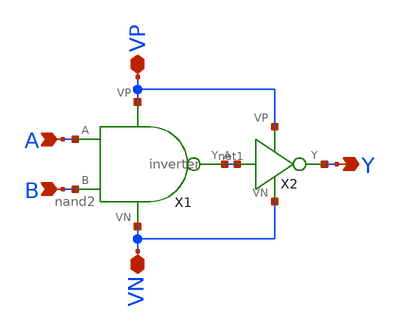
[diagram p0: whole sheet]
** sch_path: and2.sch
**.subckt and2 A B VP VN Y
*.ipin A
*.ipin B
*.iopin VP
*.iopin VN
*.opin Y
X1 B A net1 VP VN nand2
X2 net1 Y VP VN inverter
**.ends

* expanding   symbol:  /home/madvlsi/Documents/mp1/nand2.sym # of pins=5
** sym_path: nand2.sym
** sch_path: nand2.sch
.subckt nand2 B A Y VP VN
*.ipin A
*.ipin B
*.iopin VP
*.iopin VN
*.opin Y
XM1 Y A net1 VN sky130_fd_pr__nfet_01v8 L=0.15 W=1 nf=1 ad='int((nf+1)/2) * W/nf * 0.29' as='int((nf+2)/2) * W/nf * 0.29'
+ pd='2*int((nf+1)/2) * (W/nf + 0.29)' ps='2*int((nf+2)/2) * (W/nf + 0.29)' nrd='0.29 / W' nrs='0.29 / W'
+ sa=0 sb=0 sd=0 mult=1 m=1
XM2 net1 B VN VN sky130_fd_pr__nfet_01v8 L=0.15 W=1 nf=1 ad='int((nf+1)/2) * W/nf * 0.29' as='int((nf+2)/2) * W/nf * 0.29'
+ pd='2*int((nf+1)/2) * (W/nf + 0.29)' ps='2*int((nf+2)/2) * (W/nf + 0.29)' nrd='0.29 / W' nrs='0.29 / W'
+ sa=0 sb=0 sd=0 mult=1 m=1
XM3 Y A VP VP sky130_fd_pr__pfet_01v8 L=0.15 W=1 nf=1 ad='int((nf+1)/2) * W/nf * 0.29' as='int((nf+2)/2) * W/nf * 0.29'
+ pd='2*int((nf+1)/2) * (W/nf + 0.29)' ps='2*int((nf+2)/2) * (W/nf + 0.29)' nrd='0.29 / W' nrs='0.29 / W'
+ sa=0 sb=0 sd=0 mult=1 m=1
XM4 Y B VP VP sky130_fd_pr__pfet_01v8 L=0.15 W=1 nf=1 ad='int((nf+1)/2) * W/nf * 0.29' as='int((nf+2)/2) * W/nf * 0.29'
+ pd='2*int((nf+1)/2) * (W/nf + 0.29)' ps='2*int((nf+2)/2) * (W/nf + 0.29)' nrd='0.29 / W' nrs='0.29 / W'
+ sa=0 sb=0 sd=0 mult=1 m=1
.ends


* expanding   symbol:  /home/madvlsi/Documents/mp1/inverter.sym # of pins=4
** sym_path: inverter.sym
** sch_path: inverter.sch
.subckt inverter A Y VP VN
*.ipin A
*.iopin VP
*.iopin VN
*.opin Y
XM1 Y A VN VN sky130_fd_pr__nfet_01v8 L=0.15 W=1 nf=1 ad='int((nf+1)/2) * W/nf * 0.29' as='int((nf+2)/2) * W/nf * 0.29'
+ pd='2*int((nf+1)/2) * (W/nf + 0.29)' ps='2*int((nf+2)/2) * (W/nf + 0.29)' nrd='0.29 / W' nrs='0.29 / W'
+ sa=0 sb=0 sd=0 mult=1 m=1
XM2 Y A VP VP sky130_fd_pr__pfet_01v8 L=0.15 W=1 nf=1 ad='int((nf+1)/2) * W/nf * 0.29' as='int((nf+2)/2) * W/nf * 0.29'
+ pd='2*int((nf+1)/2) * (W/nf + 0.29)' ps='2*int((nf+2)/2) * (W/nf + 0.29)' nrd='0.29 / W' nrs='0.29 / W'
+ sa=0 sb=0 sd=0 mult=1 m=1
.ends

.end
